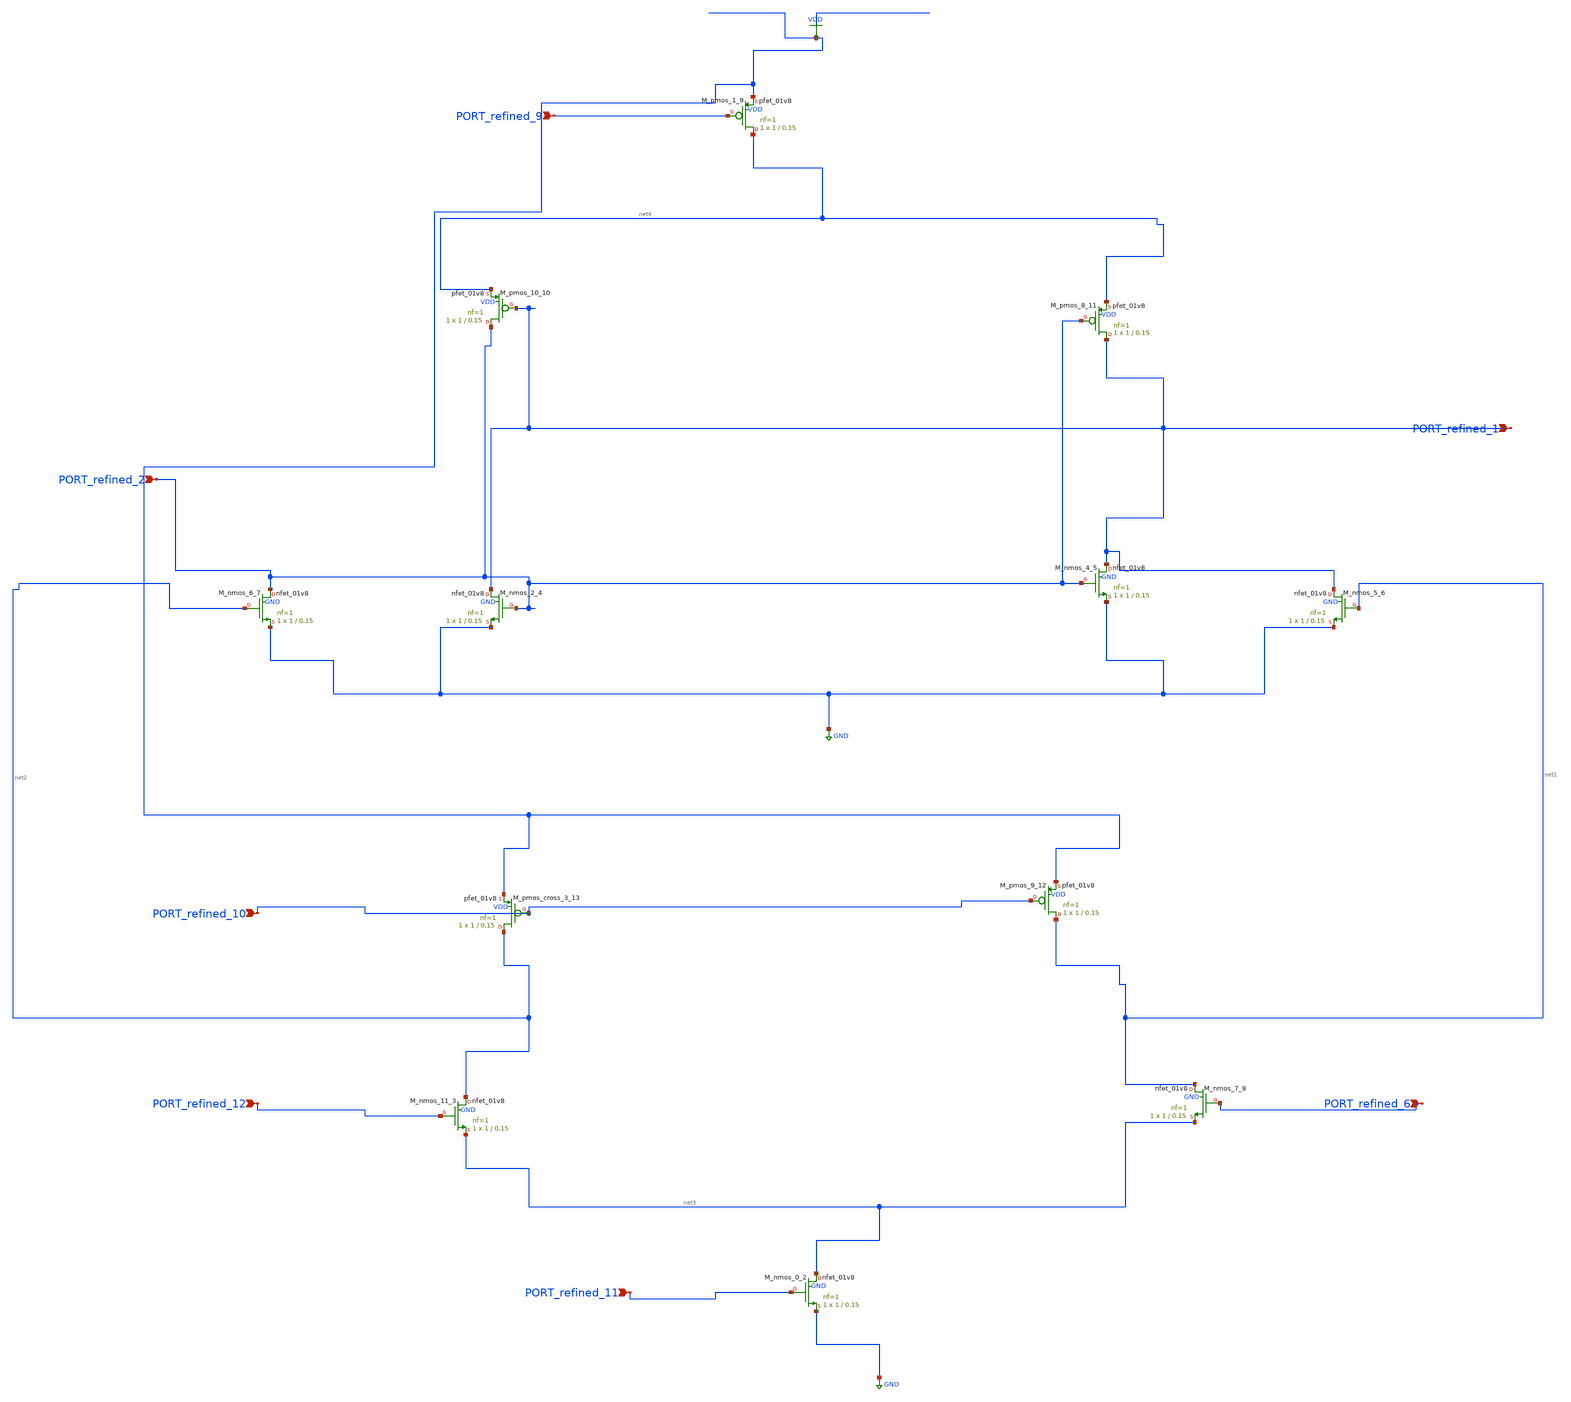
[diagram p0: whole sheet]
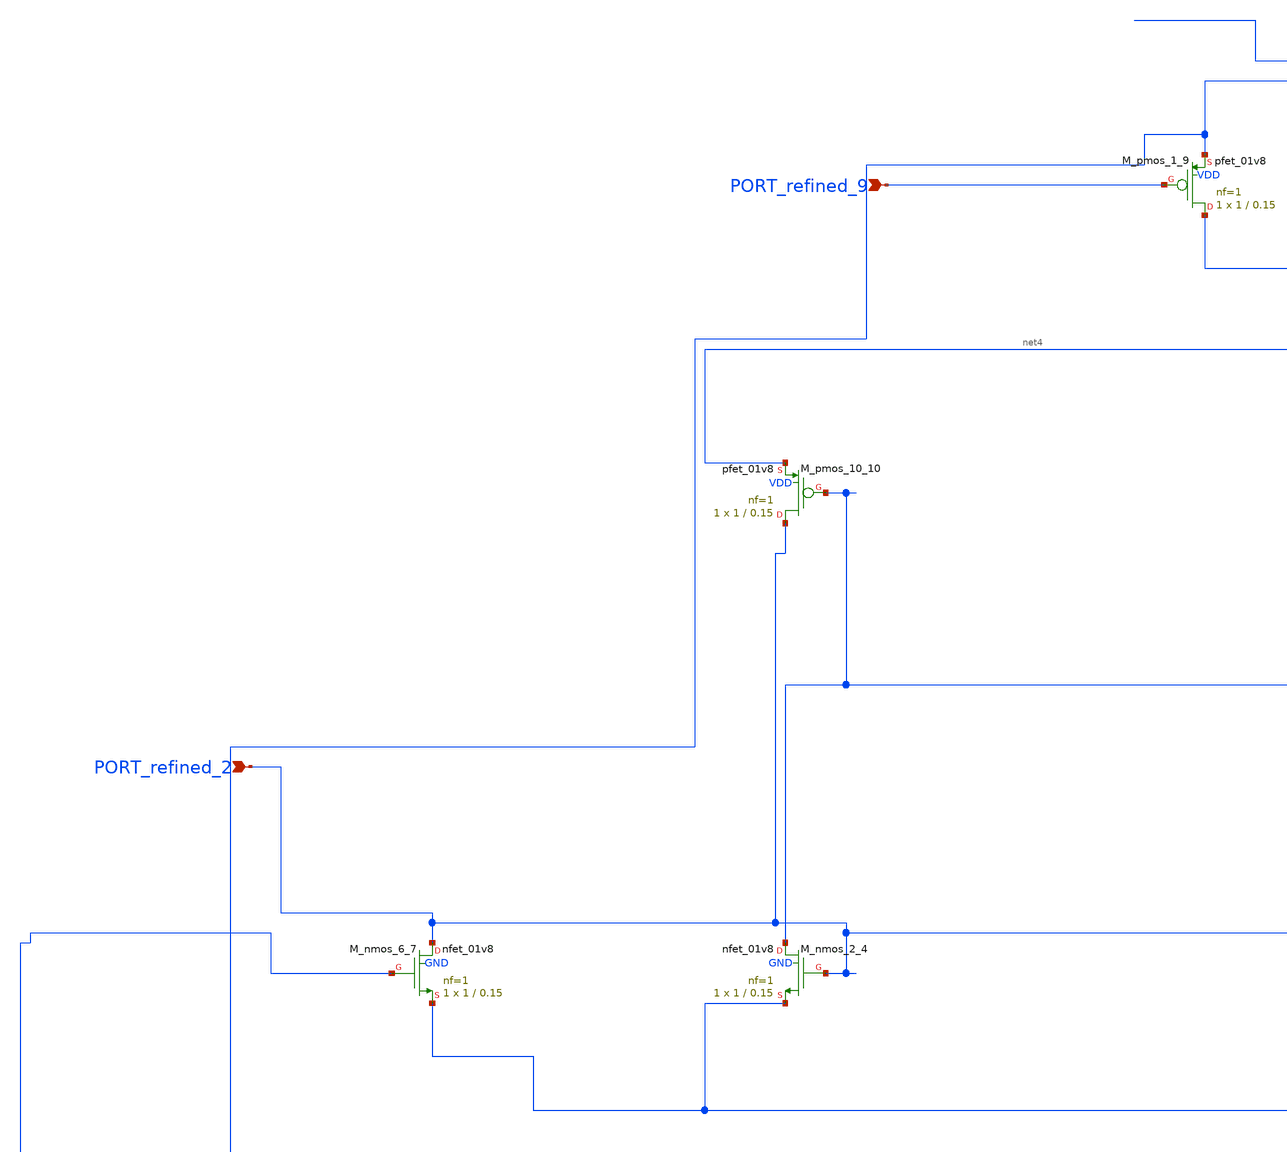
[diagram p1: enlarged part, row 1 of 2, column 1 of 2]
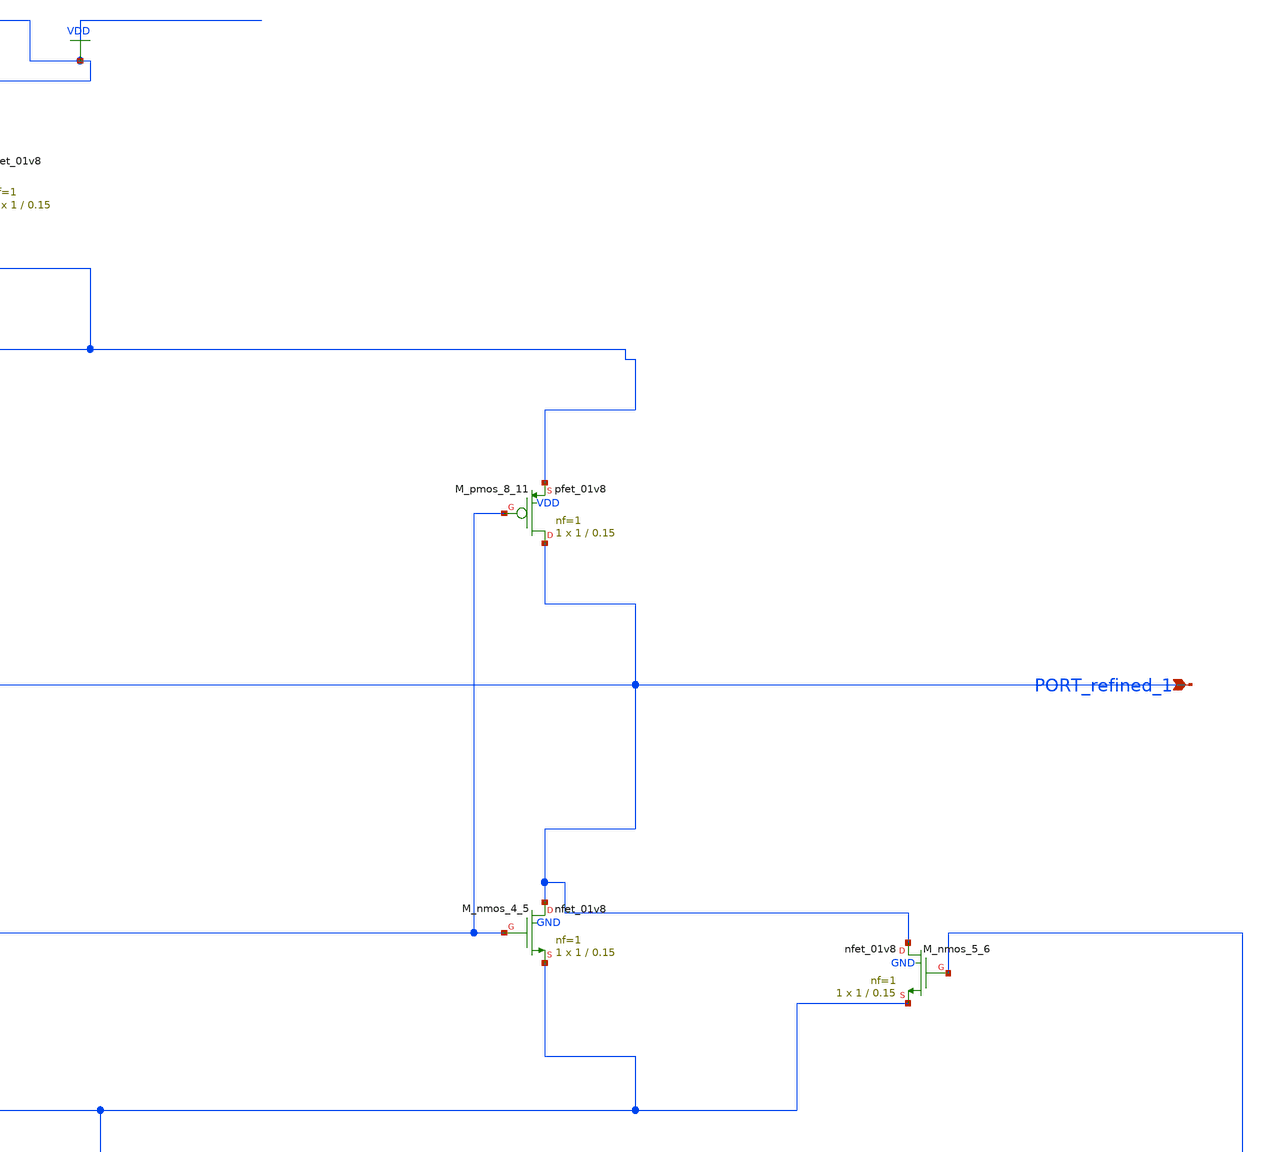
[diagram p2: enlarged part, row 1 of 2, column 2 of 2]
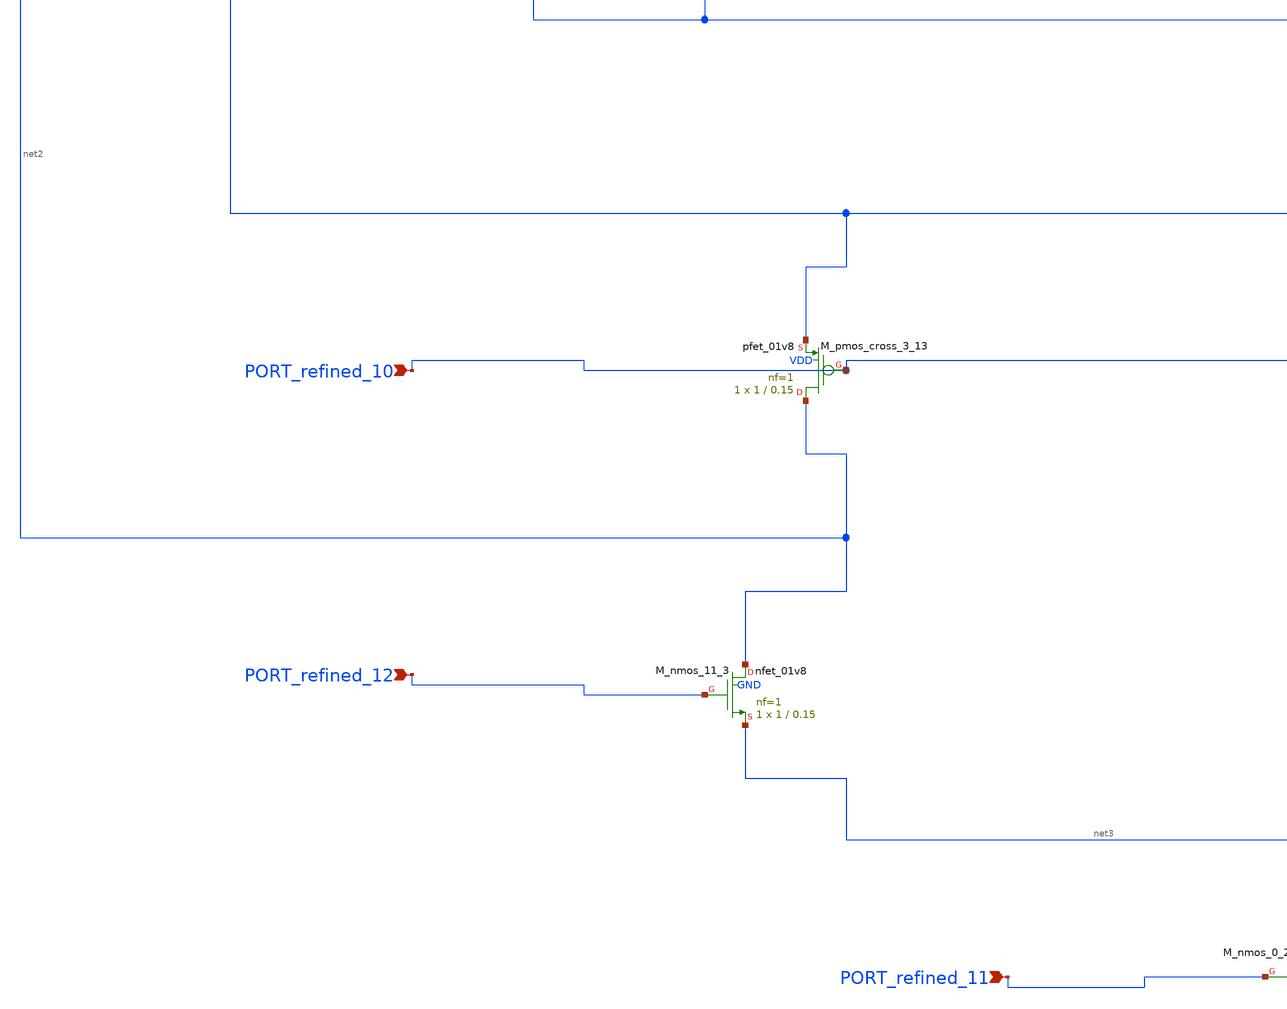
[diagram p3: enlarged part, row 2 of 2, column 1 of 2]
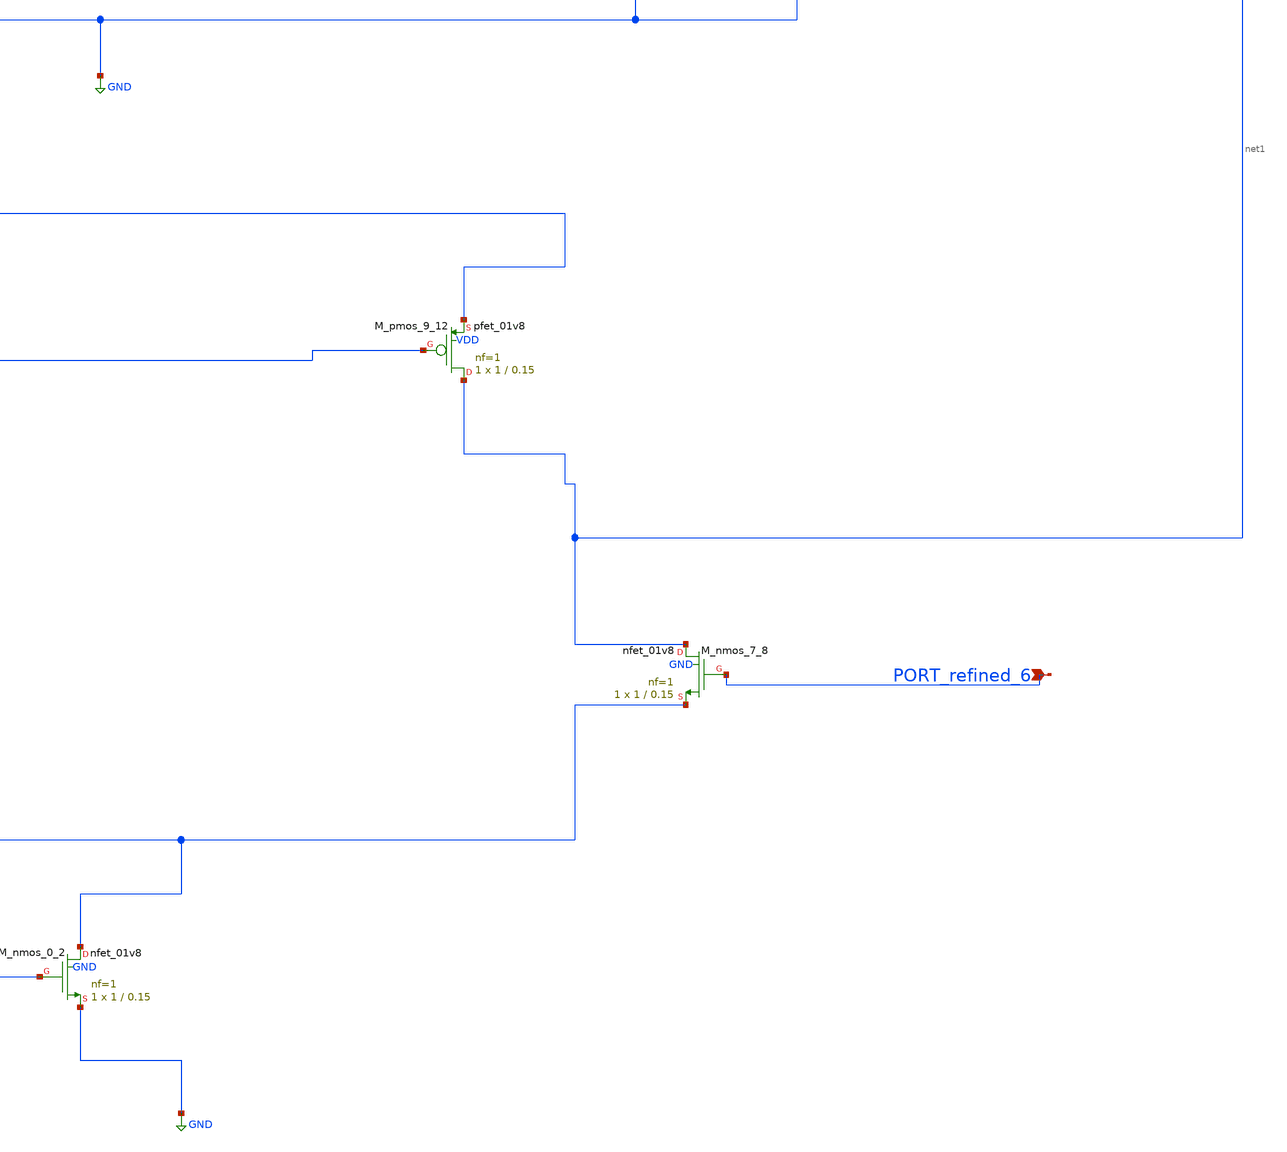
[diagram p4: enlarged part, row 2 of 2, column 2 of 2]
** sch_path: schematics/Image2Net/118.sch
**.subckt 118 PORT_refined_1 PORT_refined_2 PORT_refined_10 PORT_refined_9 PORT_refined_12
*+ PORT_refined_11 PORT_refined_6
*.ipin PORT_refined_1
*.ipin PORT_refined_2
*.ipin PORT_refined_10
*.ipin PORT_refined_9
*.ipin PORT_refined_12
*.ipin PORT_refined_11
*.ipin PORT_refined_6
XM_nmos_0_2 net3 PORT_refined_11 GND GND sky130_fd_pr__nfet_01v8 L=0.15 W=1 nf=1 ad='int((1 + 1)/2) * 1 / 1 * 0.29'
+ as='int((1 + 2)/2) * 1 / 1 * 0.29' pd='2*int((1 + 1)/2) * (1 / 1 + 0.29)' ps='2*int((1 + 2)/2) * (1 / 1 + 0.29)'
+ nrd='0.29 / 1 ' nrs='0.29 / 1 ' sa=0 sb=0 sd=0 mult=1 m=1
XM_nmos_11_3 net2 PORT_refined_12 net3 GND sky130_fd_pr__nfet_01v8 L=0.15 W=1 nf=1 ad='int((1 + 1)/2) * 1 / 1 * 0.29'
+ as='int((1 + 2)/2) * 1 / 1 * 0.29' pd='2*int((1 + 1)/2) * (1 / 1 + 0.29)' ps='2*int((1 + 2)/2) * (1 / 1 + 0.29)'
+ nrd='0.29 / 1 ' nrs='0.29 / 1 ' sa=0 sb=0 sd=0 mult=1 m=1
XM_nmos_2_4 PORT_refined_1 PORT_refined_2 GND GND sky130_fd_pr__nfet_01v8 L=0.15 W=1 nf=1 ad='int((1 + 1)/2) * 1 / 1 * 0.29'
+ as='int((1 + 2)/2) * 1 / 1 * 0.29' pd='2*int((1 + 1)/2) * (1 / 1 + 0.29)' ps='2*int((1 + 2)/2) * (1 / 1 + 0.29)'
+ nrd='0.29 / 1 ' nrs='0.29 / 1 ' sa=0 sb=0 sd=0 mult=1 m=1
XM_nmos_4_5 PORT_refined_1 PORT_refined_2 GND GND sky130_fd_pr__nfet_01v8 L=0.15 W=1 nf=1 ad='int((1 + 1)/2) * 1 / 1 * 0.29'
+ as='int((1 + 2)/2) * 1 / 1 * 0.29' pd='2*int((1 + 1)/2) * (1 / 1 + 0.29)' ps='2*int((1 + 2)/2) * (1 / 1 + 0.29)'
+ nrd='0.29 / 1 ' nrs='0.29 / 1 ' sa=0 sb=0 sd=0 mult=1 m=1
XM_nmos_5_6 PORT_refined_1 net1 GND GND sky130_fd_pr__nfet_01v8 L=0.15 W=1 nf=1 ad='int((1 + 1)/2) * 1 / 1 * 0.29'
+ as='int((1 + 2)/2) * 1 / 1 * 0.29' pd='2*int((1 + 1)/2) * (1 / 1 + 0.29)' ps='2*int((1 + 2)/2) * (1 / 1 + 0.29)'
+ nrd='0.29 / 1 ' nrs='0.29 / 1 ' sa=0 sb=0 sd=0 mult=1 m=1
XM_nmos_6_7 PORT_refined_2 net2 GND GND sky130_fd_pr__nfet_01v8 L=0.15 W=1 nf=1 ad='int((1 + 1)/2) * 1 / 1 * 0.29'
+ as='int((1 + 2)/2) * 1 / 1 * 0.29' pd='2*int((1 + 1)/2) * (1 / 1 + 0.29)' ps='2*int((1 + 2)/2) * (1 / 1 + 0.29)'
+ nrd='0.29 / 1 ' nrs='0.29 / 1 ' sa=0 sb=0 sd=0 mult=1 m=1
XM_nmos_7_8 net1 PORT_refined_6 net3 GND sky130_fd_pr__nfet_01v8 L=0.15 W=1 nf=1 ad='int((1 + 1)/2) * 1 / 1 * 0.29'
+ as='int((1 + 2)/2) * 1 / 1 * 0.29' pd='2*int((1 + 1)/2) * (1 / 1 + 0.29)' ps='2*int((1 + 2)/2) * (1 / 1 + 0.29)'
+ nrd='0.29 / 1 ' nrs='0.29 / 1 ' sa=0 sb=0 sd=0 mult=1 m=1
XM_pmos_1_9 net4 PORT_refined_9 VDD VDD sky130_fd_pr__pfet_01v8 L=0.15 W=1 nf=1 ad='int((1 + 1)/2) * 1 / 1 * 0.29'
+ as='int((1 + 2)/2) * 1 / 1 * 0.29' pd='2*int((1 + 1)/2) * (1 / 1 + 0.29)' ps='2*int((1 + 2)/2) * (1 / 1 + 0.29)'
+ nrd='0.29 / 1 ' nrs='0.29 / 1 ' sa=0 sb=0 sd=0 mult=1 m=1
XM_pmos_10_10 PORT_refined_2 PORT_refined_1 net4 VDD sky130_fd_pr__pfet_01v8 L=0.15 W=1 nf=1 ad='int((1 + 1)/2) * 1 / 1 * 0.29'
+ as='int((1 + 2)/2) * 1 / 1 * 0.29' pd='2*int((1 + 1)/2) * (1 / 1 + 0.29)' ps='2*int((1 + 2)/2) * (1 / 1 + 0.29)'
+ nrd='0.29 / 1 ' nrs='0.29 / 1 ' sa=0 sb=0 sd=0 mult=1 m=1
XM_pmos_8_11 PORT_refined_1 PORT_refined_2 net4 VDD sky130_fd_pr__pfet_01v8 L=0.15 W=1 nf=1 ad='int((1 + 1)/2) * 1 / 1 * 0.29'
+ as='int((1 + 2)/2) * 1 / 1 * 0.29' pd='2*int((1 + 1)/2) * (1 / 1 + 0.29)' ps='2*int((1 + 2)/2) * (1 / 1 + 0.29)'
+ nrd='0.29 / 1 ' nrs='0.29 / 1 ' sa=0 sb=0 sd=0 mult=1 m=1
XM_pmos_9_12 net1 PORT_refined_10 VDD VDD sky130_fd_pr__pfet_01v8 L=0.15 W=1 nf=1 ad='int((1 + 1)/2) * 1 / 1 * 0.29'
+ as='int((1 + 2)/2) * 1 / 1 * 0.29' pd='2*int((1 + 1)/2) * (1 / 1 + 0.29)' ps='2*int((1 + 2)/2) * (1 / 1 + 0.29)'
+ nrd='0.29 / 1 ' nrs='0.29 / 1 ' sa=0 sb=0 sd=0 mult=1 m=1
XM_pmos_cross_3_13 net2 PORT_refined_10 VDD VDD sky130_fd_pr__pfet_01v8 L=0.15 W=1 nf=1 ad='int((1 + 1)/2) * 1 / 1 * 0.29'
+ as='int((1 + 2)/2) * 1 / 1 * 0.29' pd='2*int((1 + 1)/2) * (1 / 1 + 0.29)' ps='2*int((1 + 2)/2) * (1 / 1 + 0.29)'
+ nrd='0.29 / 1 ' nrs='0.29 / 1 ' sa=0 sb=0 sd=0 mult=1 m=1
**.ends
.GLOBAL GND
.GLOBAL VDD
.end
